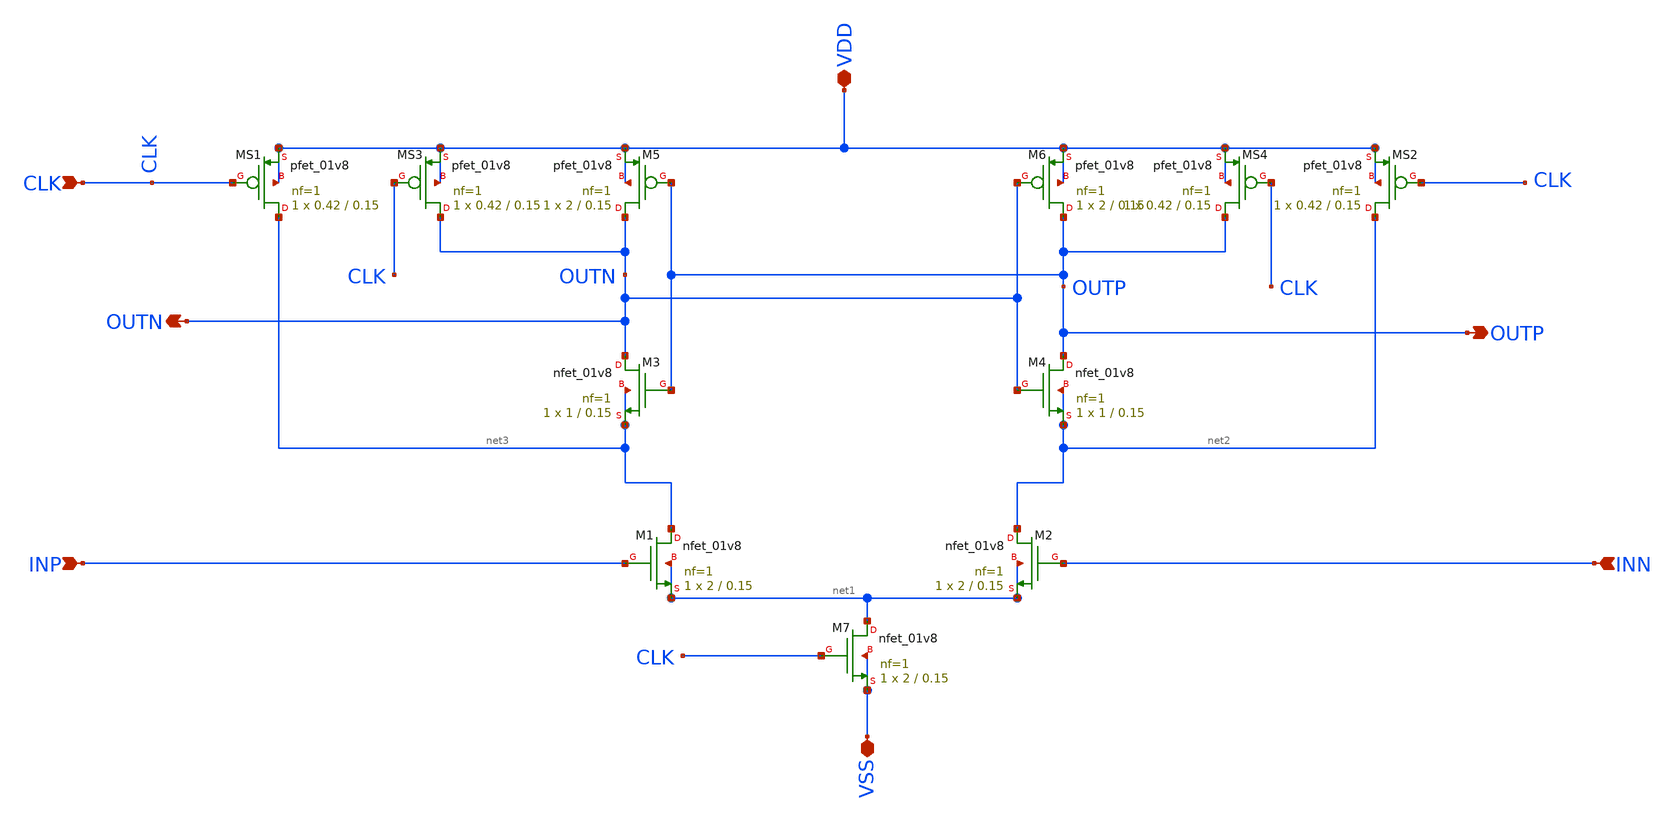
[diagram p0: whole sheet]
** sch_path: schematics/strongarm.sch
**.subckt strongarm CLK INP INN OUTP OUTN VSS VDD
*.ipin CLK
*.ipin INP
*.ipin INN
*.opin OUTP
*.opin OUTN
*.iopin VSS
*.iopin VDD
XM7 net1 CLK VSS VSS sky130_fd_pr__nfet_01v8 L=0.15 W=2 nf=1 ad='int((1 + 1)/2) * 2 / 1 * 0.29' as='int((1 + 2)/2) * 2 / 1 * 0.29'
+ pd='2*int((1 + 1)/2) * (2 / 1 + 0.29)' ps='2*int((1 + 2)/2) * (2 / 1 + 0.29)' nrd='0.29 / 2 ' nrs='0.29 / 2 '
+ sa=0 sb=0 sd=0 mult=1 m=1
XM1 net3 INP net1 net1 sky130_fd_pr__nfet_01v8 L=0.15 W=2 nf=1 ad='int((1 + 1)/2) * 2 / 1 * 0.29' as='int((1 + 2)/2) * 2 / 1 * 0.29'
+ pd='2*int((1 + 1)/2) * (2 / 1 + 0.29)' ps='2*int((1 + 2)/2) * (2 / 1 + 0.29)' nrd='0.29 / 2 ' nrs='0.29 / 2 '
+ sa=0 sb=0 sd=0 mult=1 m=1
XM2 net2 INN net1 net1 sky130_fd_pr__nfet_01v8 L=0.15 W=2 nf=1 ad='int((1 + 1)/2) * 2 / 1 * 0.29' as='int((1 + 2)/2) * 2 / 1 * 0.29'
+ pd='2*int((1 + 1)/2) * (2 / 1 + 0.29)' ps='2*int((1 + 2)/2) * (2 / 1 + 0.29)' nrd='0.29 / 2 ' nrs='0.29 / 2 '
+ sa=0 sb=0 sd=0 mult=1 m=1
XM3 OUTN OUTP net3 net3 sky130_fd_pr__nfet_01v8 L=0.15 W=1 nf=1 ad='int((1 + 1)/2) * 1 / 1 * 0.29' as='int((1 + 2)/2) * 1 / 1 * 0.29'
+ pd='2*int((1 + 1)/2) * (1 / 1 + 0.29)' ps='2*int((1 + 2)/2) * (1 / 1 + 0.29)' nrd='0.29 / 1 ' nrs='0.29 / 1 '
+ sa=0 sb=0 sd=0 mult=1 m=1
XM4 OUTP OUTN net2 net2 sky130_fd_pr__nfet_01v8 L=0.15 W=1 nf=1 ad='int((1 + 1)/2) * 1 / 1 * 0.29' as='int((1 + 2)/2) * 1 / 1 * 0.29'
+ pd='2*int((1 + 1)/2) * (1 / 1 + 0.29)' ps='2*int((1 + 2)/2) * (1 / 1 + 0.29)' nrd='0.29 / 1 ' nrs='0.29 / 1 '
+ sa=0 sb=0 sd=0 mult=1 m=1
XM5 OUTN OUTP VDD VDD sky130_fd_pr__pfet_01v8 L=0.15 W=2 nf=1 ad='int((1 + 1)/2) * 2 / 1 * 0.29' as='int((1 + 2)/2) * 2 / 1 * 0.29'
+ pd='2*int((1 + 1)/2) * (2 / 1 + 0.29)' ps='2*int((1 + 2)/2) * (2 / 1 + 0.29)' nrd='0.29 / 2 ' nrs='0.29 / 2 '
+ sa=0 sb=0 sd=0 mult=1 m=1
XM6 OUTP OUTN VDD VDD sky130_fd_pr__pfet_01v8 L=0.15 W=2 nf=1 ad='int((1 + 1)/2) * 2 / 1 * 0.29' as='int((1 + 2)/2) * 2 / 1 * 0.29'
+ pd='2*int((1 + 1)/2) * (2 / 1 + 0.29)' ps='2*int((1 + 2)/2) * (2 / 1 + 0.29)' nrd='0.29 / 2 ' nrs='0.29 / 2 '
+ sa=0 sb=0 sd=0 mult=1 m=1
XMS3 OUTN CLK VDD VDD sky130_fd_pr__pfet_01v8 L=0.15 W=0.42 nf=1 ad='int((1 + 1)/2) * 0.42 / 1 * 0.29'
+ as='int((1 + 2)/2) * 0.42 / 1 * 0.29' pd='2*int((1 + 1)/2) * (0.42 / 1 + 0.29)' ps='2*int((1 + 2)/2) * (0.42 / 1 + 0.29)'
+ nrd='0.29 / 0.42 ' nrs='0.29 / 0.42 ' sa=0 sb=0 sd=0 mult=1 m=1
XMS1 net3 CLK VDD VDD sky130_fd_pr__pfet_01v8 L=0.15 W=0.42 nf=1 ad='int((1 + 1)/2) * 0.42 / 1 * 0.29'
+ as='int((1 + 2)/2) * 0.42 / 1 * 0.29' pd='2*int((1 + 1)/2) * (0.42 / 1 + 0.29)' ps='2*int((1 + 2)/2) * (0.42 / 1 + 0.29)'
+ nrd='0.29 / 0.42 ' nrs='0.29 / 0.42 ' sa=0 sb=0 sd=0 mult=1 m=1
XMS4 OUTP CLK VDD VDD sky130_fd_pr__pfet_01v8 L=0.15 W=0.42 nf=1 ad='int((1 + 1)/2) * 0.42 / 1 * 0.29'
+ as='int((1 + 2)/2) * 0.42 / 1 * 0.29' pd='2*int((1 + 1)/2) * (0.42 / 1 + 0.29)' ps='2*int((1 + 2)/2) * (0.42 / 1 + 0.29)'
+ nrd='0.29 / 0.42 ' nrs='0.29 / 0.42 ' sa=0 sb=0 sd=0 mult=1 m=1
XMS2 net2 CLK VDD VDD sky130_fd_pr__pfet_01v8 L=0.15 W=0.42 nf=1 ad='int((1 + 1)/2) * 0.42 / 1 * 0.29'
+ as='int((1 + 2)/2) * 0.42 / 1 * 0.29' pd='2*int((1 + 1)/2) * (0.42 / 1 + 0.29)' ps='2*int((1 + 2)/2) * (0.42 / 1 + 0.29)'
+ nrd='0.29 / 0.42 ' nrs='0.29 / 0.42 ' sa=0 sb=0 sd=0 mult=1 m=1
**.ends
.end
